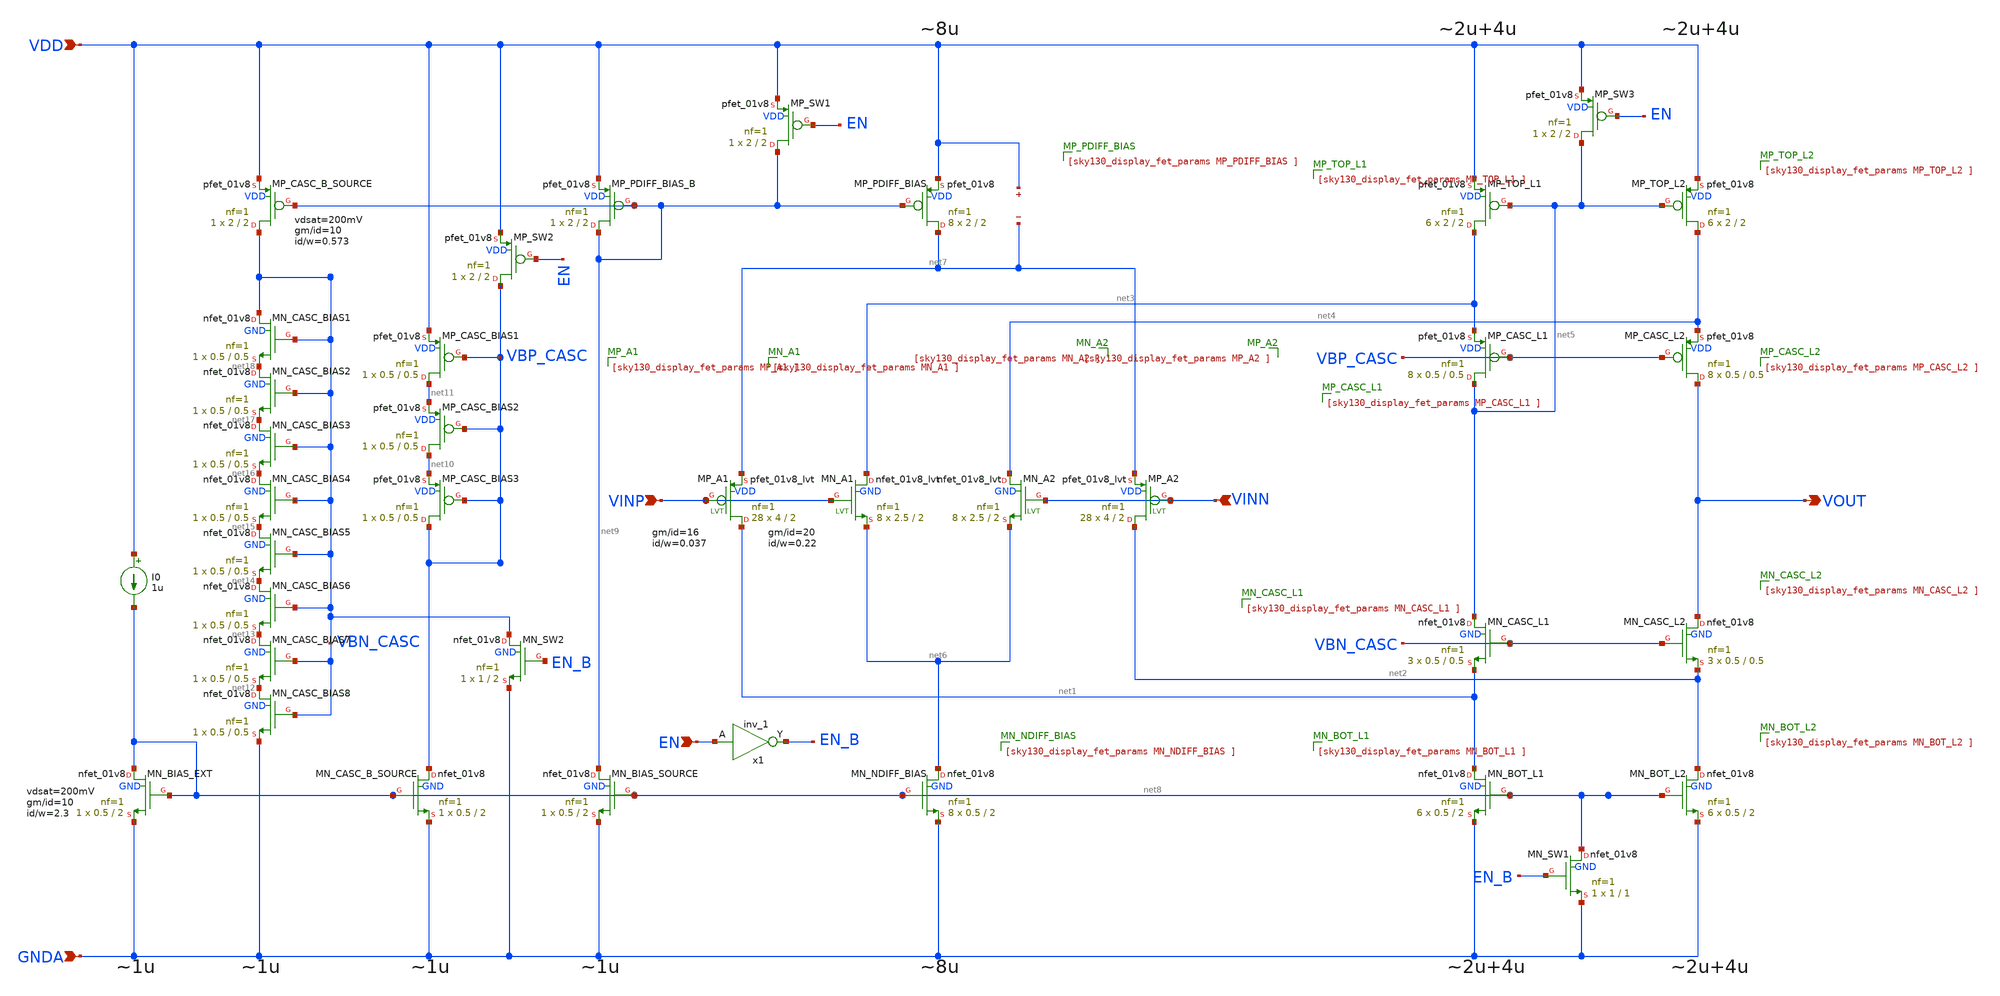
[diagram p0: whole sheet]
** sch_path: OTAs/Rail_to_Rail_IP_OP_SWING_OTA__IP/SCH/Rail_to_Rail_IP_OP_OTA.sch
**.subckt Rail_to_Rail_IP_OP_OTA VINP VINN VDD GNDA VOUT EN
*.ipin VINP
*.ipin VINN
*.ipin VDD
*.ipin GNDA
*.opin VOUT
*.ipin EN
XMN_BOT_L2 net2 net8 GNDA GND sky130_fd_pr__nfet_01v8 L=2 W=0.5 nf=1 ad='int((1 + 1)/2) * 0.5 / 1 * 0.29'
+ as='int((1 + 2)/2) * 0.5 / 1 * 0.29' pd='2*int((1 + 1)/2) * (0.5 / 1 + 0.29)' ps='2*int((1 + 2)/2) * (0.5 / 1 + 0.29)'
+ nrd='0.29 / 0.5 ' nrs='0.29 / 0.5 ' sa=0 sb=0 sd=0 mult=6 m=6
XMN_CASC_L2 VOUT VBN_CASC net2 GND sky130_fd_pr__nfet_01v8 L=0.5 W=0.5 nf=1 ad='int((1 + 1)/2) * 0.5 / 1 * 0.29'
+ as='int((1 + 2)/2) * 0.5 / 1 * 0.29' pd='2*int((1 + 1)/2) * (0.5 / 1 + 0.29)' ps='2*int((1 + 2)/2) * (0.5 / 1 + 0.29)'
+ nrd='0.29 / 0.5 ' nrs='0.29 / 0.5 ' sa=0 sb=0 sd=0 mult=3 m=3
XMN_BOT_L1 net1 net8 GNDA GND sky130_fd_pr__nfet_01v8 L=2 W=0.5 nf=1 ad='int((1 + 1)/2) * 0.5 / 1 * 0.29'
+ as='int((1 + 2)/2) * 0.5 / 1 * 0.29' pd='2*int((1 + 1)/2) * (0.5 / 1 + 0.29)' ps='2*int((1 + 2)/2) * (0.5 / 1 + 0.29)'
+ nrd='0.29 / 0.5 ' nrs='0.29 / 0.5 ' sa=0 sb=0 sd=0 mult=6 m=6
XMN_CASC_L1 net5 VBN_CASC net1 GND sky130_fd_pr__nfet_01v8 L=0.5 W=0.5 nf=1 ad='int((1 + 1)/2) * 0.5 / 1 * 0.29'
+ as='int((1 + 2)/2) * 0.5 / 1 * 0.29' pd='2*int((1 + 1)/2) * (0.5 / 1 + 0.29)' ps='2*int((1 + 2)/2) * (0.5 / 1 + 0.29)'
+ nrd='0.29 / 0.5 ' nrs='0.29 / 0.5 ' sa=0 sb=0 sd=0 mult=3 m=3
XMP_CASC_L2 VOUT VBP_CASC net4 VDD sky130_fd_pr__pfet_01v8 L=0.5 W=0.5 nf=1 ad='int((1 + 1)/2) * 0.5 / 1 * 0.29'
+ as='int((1 + 2)/2) * 0.5 / 1 * 0.29' pd='2*int((1 + 1)/2) * (0.5 / 1 + 0.29)' ps='2*int((1 + 2)/2) * (0.5 / 1 + 0.29)'
+ nrd='0.29 / 0.5 ' nrs='0.29 / 0.5 ' sa=0 sb=0 sd=0 mult=8 m=8
XMP_CASC_L1 net5 VBP_CASC net3 VDD sky130_fd_pr__pfet_01v8 L=0.5 W=0.5 nf=1 ad='int((1 + 1)/2) * 0.5 / 1 * 0.29'
+ as='int((1 + 2)/2) * 0.5 / 1 * 0.29' pd='2*int((1 + 1)/2) * (0.5 / 1 + 0.29)' ps='2*int((1 + 2)/2) * (0.5 / 1 + 0.29)'
+ nrd='0.29 / 0.5 ' nrs='0.29 / 0.5 ' sa=0 sb=0 sd=0 mult=8 m=8
XMP_TOP_L1 net3 net5 VDD VDD sky130_fd_pr__pfet_01v8 L=2 W=2 nf=1 ad='int((1 + 1)/2) * 2 / 1 * 0.29'
+ as='int((1 + 2)/2) * 2 / 1 * 0.29' pd='2*int((1 + 1)/2) * (2 / 1 + 0.29)' ps='2*int((1 + 2)/2) * (2 / 1 + 0.29)'
+ nrd='0.29 / 2 ' nrs='0.29 / 2 ' sa=0 sb=0 sd=0 mult=6 m=6
XMN_A1 net3 VINP net6 GND sky130_fd_pr__nfet_01v8_lvt L=2 W=2.5 nf=1 ad='int((1 + 1)/2) * 2.5 / 1 * 0.29'
+ as='int((1 + 2)/2) * 2.5 / 1 * 0.29' pd='2*int((1 + 1)/2) * (2.5 / 1 + 0.29)' ps='2*int((1 + 2)/2) * (2.5 / 1 + 0.29)'
+ nrd='0.29 / 2.5 ' nrs='0.29 / 2.5 ' sa=0 sb=0 sd=0 mult=8 m=8
XMN_A2 net4 VINN net6 GND sky130_fd_pr__nfet_01v8_lvt L=2 W=2.5 nf=1 ad='int((1 + 1)/2) * 2.5 / 1 * 0.29'
+ as='int((1 + 2)/2) * 2.5 / 1 * 0.29' pd='2*int((1 + 1)/2) * (2.5 / 1 + 0.29)' ps='2*int((1 + 2)/2) * (2.5 / 1 + 0.29)'
+ nrd='0.29 / 2.5 ' nrs='0.29 / 2.5 ' sa=0 sb=0 sd=0 mult=8 m=8
XMP_A1 net1 VINP net7 VDD sky130_fd_pr__pfet_01v8_lvt L=2 W=4 nf=1 ad='int((1 + 1)/2) * 4 / 1 * 0.29'
+ as='int((1 + 2)/2) * 4 / 1 * 0.29' pd='2*int((1 + 1)/2) * (4 / 1 + 0.29)' ps='2*int((1 + 2)/2) * (4 / 1 + 0.29)'
+ nrd='0.29 / 4 ' nrs='0.29 / 4 ' sa=0 sb=0 sd=0 mult=28 m=28
XMP_A2 net2 VINN net7 VDD sky130_fd_pr__pfet_01v8_lvt L=2 W=4 nf=1 ad='int((1 + 1)/2) * 4 / 1 * 0.29'
+ as='int((1 + 2)/2) * 4 / 1 * 0.29' pd='2*int((1 + 1)/2) * (4 / 1 + 0.29)' ps='2*int((1 + 2)/2) * (4 / 1 + 0.29)'
+ nrd='0.29 / 4 ' nrs='0.29 / 4 ' sa=0 sb=0 sd=0 mult=28 m=28
XMP_PDIFF_BIAS net7 net9 VDD VDD sky130_fd_pr__pfet_01v8 L=2 W=2 nf=1 ad='int((1 + 1)/2) * 2 / 1 * 0.29'
+ as='int((1 + 2)/2) * 2 / 1 * 0.29' pd='2*int((1 + 1)/2) * (2 / 1 + 0.29)' ps='2*int((1 + 2)/2) * (2 / 1 + 0.29)'
+ nrd='0.29 / 2 ' nrs='0.29 / 2 ' sa=0 sb=0 sd=0 mult=8 m=8
XMN_NDIFF_BIAS net6 net8 GNDA GND sky130_fd_pr__nfet_01v8 L=2 W=0.5 nf=1 ad='int((1 + 1)/2) * 0.5 / 1 * 0.29'
+ as='int((1 + 2)/2) * 0.5 / 1 * 0.29' pd='2*int((1 + 1)/2) * (0.5 / 1 + 0.29)' ps='2*int((1 + 2)/2) * (0.5 / 1 + 0.29)'
+ nrd='0.29 / 0.5 ' nrs='0.29 / 0.5 ' sa=0 sb=0 sd=0 mult=8 m=8
XMP_PDIFF_BIAS_B net9 net9 VDD VDD sky130_fd_pr__pfet_01v8 L=2 W=2 nf=1 ad='int((1 + 1)/2) * 2 / 1 * 0.29'
+ as='int((1 + 2)/2) * 2 / 1 * 0.29' pd='2*int((1 + 1)/2) * (2 / 1 + 0.29)' ps='2*int((1 + 2)/2) * (2 / 1 + 0.29)'
+ nrd='0.29 / 2 ' nrs='0.29 / 2 ' sa=0 sb=0 sd=0 mult=1 m=1
XMP_TOP_L2 net4 net5 VDD VDD sky130_fd_pr__pfet_01v8 L=2 W=2 nf=1 ad='int((1 + 1)/2) * 2 / 1 * 0.29'
+ as='int((1 + 2)/2) * 2 / 1 * 0.29' pd='2*int((1 + 1)/2) * (2 / 1 + 0.29)' ps='2*int((1 + 2)/2) * (2 / 1 + 0.29)'
+ nrd='0.29 / 2 ' nrs='0.29 / 2 ' sa=0 sb=0 sd=0 mult=6 m=6
XMN_BIAS_SOURCE net9 net8 GNDA GND sky130_fd_pr__nfet_01v8 L=2 W=0.5 nf=1 ad='int((1 + 1)/2) * 0.5 / 1 * 0.29'
+ as='int((1 + 2)/2) * 0.5 / 1 * 0.29' pd='2*int((1 + 1)/2) * (0.5 / 1 + 0.29)' ps='2*int((1 + 2)/2) * (0.5 / 1 + 0.29)'
+ nrd='0.29 / 0.5 ' nrs='0.29 / 0.5 ' sa=0 sb=0 sd=0 mult=1 m=1
XMN_BIAS_EXT net8 net8 GNDA GND sky130_fd_pr__nfet_01v8 L=2 W=0.5 nf=1 ad='int((1 + 1)/2) * 0.5 / 1 * 0.29'
+ as='int((1 + 2)/2) * 0.5 / 1 * 0.29' pd='2*int((1 + 1)/2) * (0.5 / 1 + 0.29)' ps='2*int((1 + 2)/2) * (0.5 / 1 + 0.29)'
+ nrd='0.29 / 0.5 ' nrs='0.29 / 0.5 ' sa=0 sb=0 sd=0 mult=1 m=1
I0 VDD net8 1u
XMP_CASC_B_SOURCE VBN_CASC net9 VDD VDD sky130_fd_pr__pfet_01v8 L=2 W=2 nf=1 ad='int((1 + 1)/2) * 2 / 1 * 0.29'
+ as='int((1 + 2)/2) * 2 / 1 * 0.29' pd='2*int((1 + 1)/2) * (2 / 1 + 0.29)' ps='2*int((1 + 2)/2) * (2 / 1 + 0.29)'
+ nrd='0.29 / 2 ' nrs='0.29 / 2 ' sa=0 sb=0 sd=0 mult=1 m=1
XMN_CASC_BIAS8 net12 VBN_CASC GNDA GND sky130_fd_pr__nfet_01v8 L=0.5 W=0.5 nf=1 ad='int((1 + 1)/2) * 0.5 / 1 * 0.29'
+ as='int((1 + 2)/2) * 0.5 / 1 * 0.29' pd='2*int((1 + 1)/2) * (0.5 / 1 + 0.29)' ps='2*int((1 + 2)/2) * (0.5 / 1 + 0.29)'
+ nrd='0.29 / 0.5 ' nrs='0.29 / 0.5 ' sa=0 sb=0 sd=0 mult=1 m=1
XMN_CASC_B_SOURCE VBP_CASC net8 GNDA GND sky130_fd_pr__nfet_01v8 L=2 W=0.5 nf=1 ad='int((1 + 1)/2) * 0.5 / 1 * 0.29'
+ as='int((1 + 2)/2) * 0.5 / 1 * 0.29' pd='2*int((1 + 1)/2) * (0.5 / 1 + 0.29)' ps='2*int((1 + 2)/2) * (0.5 / 1 + 0.29)'
+ nrd='0.29 / 0.5 ' nrs='0.29 / 0.5 ' sa=0 sb=0 sd=0 mult=1 m=1
XMP_CASC_BIAS1 net11 VBP_CASC VDD VDD sky130_fd_pr__pfet_01v8 L=0.5 W=0.5 nf=1 ad='int((1 + 1)/2) * 0.5 / 1 * 0.29'
+ as='int((1 + 2)/2) * 0.5 / 1 * 0.29' pd='2*int((1 + 1)/2) * (0.5 / 1 + 0.29)' ps='2*int((1 + 2)/2) * (0.5 / 1 + 0.29)'
+ nrd='0.29 / 0.5 ' nrs='0.29 / 0.5 ' sa=0 sb=0 sd=0 mult=1 m=1
XMN_CASC_BIAS7 net13 VBN_CASC net12 GND sky130_fd_pr__nfet_01v8 L=0.5 W=0.5 nf=1 ad='int((1 + 1)/2) * 0.5 / 1 * 0.29'
+ as='int((1 + 2)/2) * 0.5 / 1 * 0.29' pd='2*int((1 + 1)/2) * (0.5 / 1 + 0.29)' ps='2*int((1 + 2)/2) * (0.5 / 1 + 0.29)'
+ nrd='0.29 / 0.5 ' nrs='0.29 / 0.5 ' sa=0 sb=0 sd=0 mult=1 m=1
XMN_CASC_BIAS6 net14 VBN_CASC net13 GND sky130_fd_pr__nfet_01v8 L=0.5 W=0.5 nf=1 ad='int((1 + 1)/2) * 0.5 / 1 * 0.29'
+ as='int((1 + 2)/2) * 0.5 / 1 * 0.29' pd='2*int((1 + 1)/2) * (0.5 / 1 + 0.29)' ps='2*int((1 + 2)/2) * (0.5 / 1 + 0.29)'
+ nrd='0.29 / 0.5 ' nrs='0.29 / 0.5 ' sa=0 sb=0 sd=0 mult=1 m=1
XMP_CASC_BIAS2 net10 VBP_CASC net11 VDD sky130_fd_pr__pfet_01v8 L=0.5 W=0.5 nf=1 ad='int((1 + 1)/2) * 0.5 / 1 * 0.29'
+ as='int((1 + 2)/2) * 0.5 / 1 * 0.29' pd='2*int((1 + 1)/2) * (0.5 / 1 + 0.29)' ps='2*int((1 + 2)/2) * (0.5 / 1 + 0.29)'
+ nrd='0.29 / 0.5 ' nrs='0.29 / 0.5 ' sa=0 sb=0 sd=0 mult=1 m=1
XMP_CASC_BIAS3 VBP_CASC VBP_CASC net10 VDD sky130_fd_pr__pfet_01v8 L=0.5 W=0.5 nf=1 ad='int((1 + 1)/2) * 0.5 / 1 * 0.29'
+ as='int((1 + 2)/2) * 0.5 / 1 * 0.29' pd='2*int((1 + 1)/2) * (0.5 / 1 + 0.29)' ps='2*int((1 + 2)/2) * (0.5 / 1 + 0.29)'
+ nrd='0.29 / 0.5 ' nrs='0.29 / 0.5 ' sa=0 sb=0 sd=0 mult=1 m=1
XMN_CASC_BIAS5 net15 VBN_CASC net14 GND sky130_fd_pr__nfet_01v8 L=0.5 W=0.5 nf=1 ad='int((1 + 1)/2) * 0.5 / 1 * 0.29'
+ as='int((1 + 2)/2) * 0.5 / 1 * 0.29' pd='2*int((1 + 1)/2) * (0.5 / 1 + 0.29)' ps='2*int((1 + 2)/2) * (0.5 / 1 + 0.29)'
+ nrd='0.29 / 0.5 ' nrs='0.29 / 0.5 ' sa=0 sb=0 sd=0 mult=1 m=1
XMN_CASC_BIAS4 net16 VBN_CASC net15 GND sky130_fd_pr__nfet_01v8 L=0.5 W=0.5 nf=1 ad='int((1 + 1)/2) * 0.5 / 1 * 0.29'
+ as='int((1 + 2)/2) * 0.5 / 1 * 0.29' pd='2*int((1 + 1)/2) * (0.5 / 1 + 0.29)' ps='2*int((1 + 2)/2) * (0.5 / 1 + 0.29)'
+ nrd='0.29 / 0.5 ' nrs='0.29 / 0.5 ' sa=0 sb=0 sd=0 mult=1 m=1
XMN_CASC_BIAS3 net17 VBN_CASC net16 GND sky130_fd_pr__nfet_01v8 L=0.5 W=0.5 nf=1 ad='int((1 + 1)/2) * 0.5 / 1 * 0.29'
+ as='int((1 + 2)/2) * 0.5 / 1 * 0.29' pd='2*int((1 + 1)/2) * (0.5 / 1 + 0.29)' ps='2*int((1 + 2)/2) * (0.5 / 1 + 0.29)'
+ nrd='0.29 / 0.5 ' nrs='0.29 / 0.5 ' sa=0 sb=0 sd=0 mult=1 m=1
XMN_CASC_BIAS1 VBN_CASC VBN_CASC net18 GND sky130_fd_pr__nfet_01v8 L=0.5 W=0.5 nf=1 ad='int((1 + 1)/2) * 0.5 / 1 * 0.29'
+ as='int((1 + 2)/2) * 0.5 / 1 * 0.29' pd='2*int((1 + 1)/2) * (0.5 / 1 + 0.29)' ps='2*int((1 + 2)/2) * (0.5 / 1 + 0.29)'
+ nrd='0.29 / 0.5 ' nrs='0.29 / 0.5 ' sa=0 sb=0 sd=0 mult=1 m=1
XMN_CASC_BIAS2 net18 VBN_CASC net17 GND sky130_fd_pr__nfet_01v8 L=0.5 W=0.5 nf=1 ad='int((1 + 1)/2) * 0.5 / 1 * 0.29'
+ as='int((1 + 2)/2) * 0.5 / 1 * 0.29' pd='2*int((1 + 1)/2) * (0.5 / 1 + 0.29)' ps='2*int((1 + 2)/2) * (0.5 / 1 + 0.29)'
+ nrd='0.29 / 0.5 ' nrs='0.29 / 0.5 ' sa=0 sb=0 sd=0 mult=1 m=1
XMN_SW1 net8 EN_B GNDA GND sky130_fd_pr__nfet_01v8 L=1 W=1 nf=1 ad='int((1 + 1)/2) * 1 / 1 * 0.29' as='int((1 + 2)/2) * 1 / 1 * 0.29'
+ pd='2*int((1 + 1)/2) * (1 / 1 + 0.29)' ps='2*int((1 + 2)/2) * (1 / 1 + 0.29)' nrd='0.29 / 1 ' nrs='0.29 / 1 '
+ sa=0 sb=0 sd=0 mult=1 m=1
XMP_SW1 net9 EN VDD VDD sky130_fd_pr__pfet_01v8 L=2 W=2 nf=1 ad='int((1 + 1)/2) * 2 / 1 * 0.29' as='int((1 + 2)/2) * 2 / 1 * 0.29'
+ pd='2*int((1 + 1)/2) * (2 / 1 + 0.29)' ps='2*int((1 + 2)/2) * (2 / 1 + 0.29)' nrd='0.29 / 2 ' nrs='0.29 / 2 '
+ sa=0 sb=0 sd=0 mult=1 m=1
x1 EN GNDA GNDA VDD VDD EN_B sky130_fd_sc_hd__inv_1
XMP_SW2 VBP_CASC EN VDD VDD sky130_fd_pr__pfet_01v8 L=2 W=2 nf=1 ad='int((1 + 1)/2) * 2 / 1 * 0.29' as='int((1 + 2)/2) * 2 / 1 * 0.29'
+ pd='2*int((1 + 1)/2) * (2 / 1 + 0.29)' ps='2*int((1 + 2)/2) * (2 / 1 + 0.29)' nrd='0.29 / 2 ' nrs='0.29 / 2 '
+ sa=0 sb=0 sd=0 mult=1 m=1
XMN_SW2 VBN_CASC EN_B GNDA GND sky130_fd_pr__nfet_01v8 L=2 W=1 nf=1 ad='int((1 + 1)/2) * 1 / 1 * 0.29'
+ as='int((1 + 2)/2) * 1 / 1 * 0.29' pd='2*int((1 + 1)/2) * (1 / 1 + 0.29)' ps='2*int((1 + 2)/2) * (1 / 1 + 0.29)'
+ nrd='0.29 / 1 ' nrs='0.29 / 1 ' sa=0 sb=0 sd=0 mult=1 m=1
XMP_SW3 net5 EN VDD VDD sky130_fd_pr__pfet_01v8 L=2 W=2 nf=1 ad='int((1 + 1)/2) * 2 / 1 * 0.29' as='int((1 + 2)/2) * 2 / 1 * 0.29'
+ pd='2*int((1 + 1)/2) * (2 / 1 + 0.29)' ps='2*int((1 + 2)/2) * (2 / 1 + 0.29)' nrd='0.29 / 2 ' nrs='0.29 / 2 '
+ sa=0 sb=0 sd=0 mult=1 m=1
.save v(vdd)
.save v(net7)
**.ends
.end
